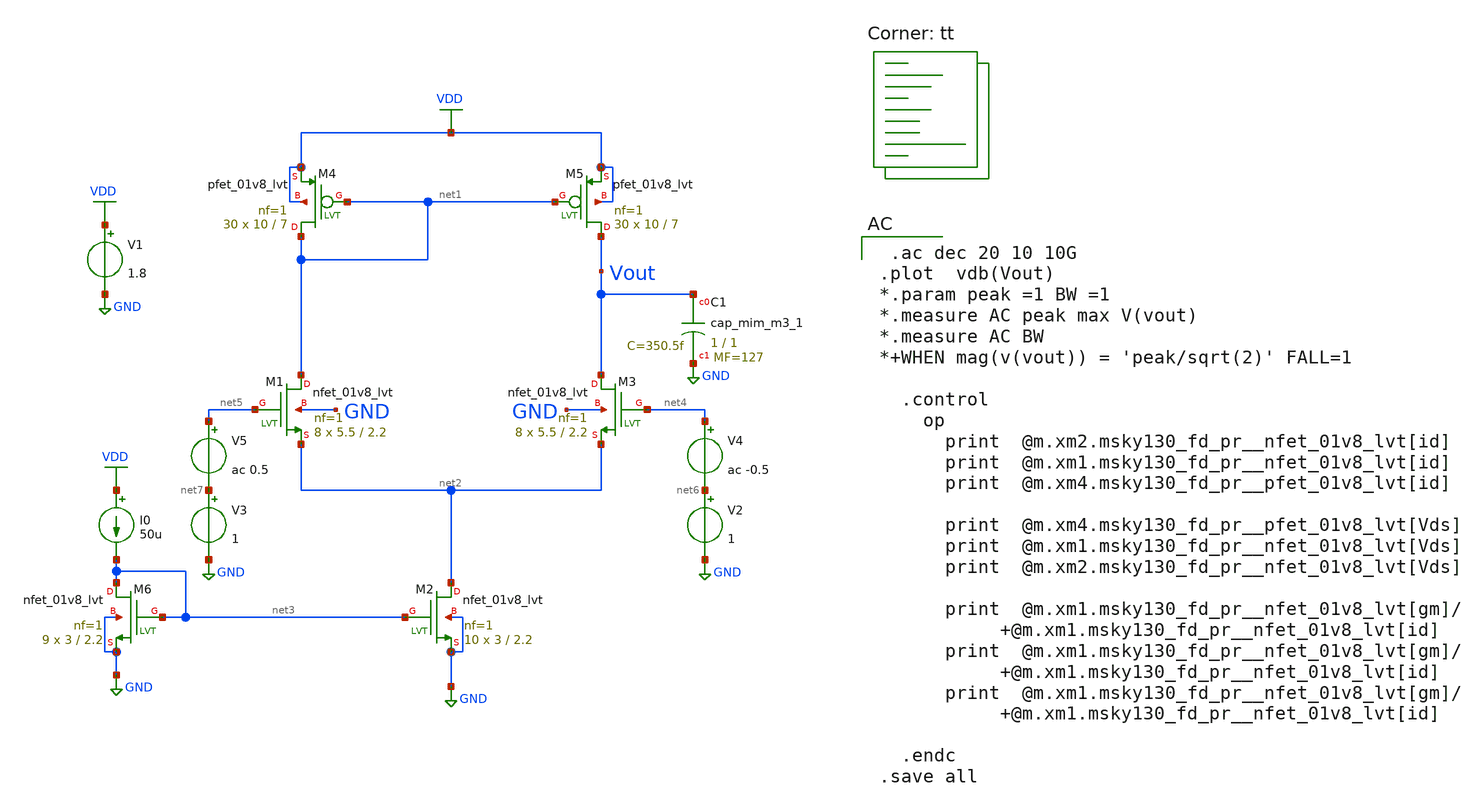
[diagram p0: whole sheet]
** sch_path: pll/lc_vco_lib_Hossam_Tarek/OTA/xschem/OTA.sch
**.subckt OTA
XM1 net1 net5 net2 GND sky130_fd_pr__nfet_01v8_lvt L=2.2 W=5.5 nf=1 ad='int((nf+1)/2) * W/nf * 0.29'
+ as='int((nf+2)/2) * W/nf * 0.29' pd='2*int((nf+1)/2) * (W/nf + 0.29)' ps='2*int((nf+2)/2) * (W/nf + 0.29)'
+ nrd='0.29 / W' nrs='0.29 / W' sa=0 sb=0 sd=0 mult=8 m=8
XM2 net2 net3 GND GND sky130_fd_pr__nfet_01v8_lvt L=2.2 W=3 nf=1 ad='int((nf+1)/2) * W/nf * 0.29' as='int((nf+2)/2) * W/nf * 0.29'
+ pd='2*int((nf+1)/2) * (W/nf + 0.29)' ps='2*int((nf+2)/2) * (W/nf + 0.29)' nrd='0.29 / W' nrs='0.29 / W'
+ sa=0 sb=0 sd=0 mult=10 m=10
XM3 Vout net4 net2 GND sky130_fd_pr__nfet_01v8_lvt L=2.2 W=5.5 nf=1 ad='int((nf+1)/2) * W/nf * 0.29'
+ as='int((nf+2)/2) * W/nf * 0.29' pd='2*int((nf+1)/2) * (W/nf + 0.29)' ps='2*int((nf+2)/2) * (W/nf + 0.29)'
+ nrd='0.29 / W' nrs='0.29 / W' sa=0 sb=0 sd=0 mult=8 m=8
XM4 net1 net1 VDD VDD sky130_fd_pr__pfet_01v8_lvt L=7 W=10 nf=1 ad='int((nf+1)/2) * W/nf * 0.29' as='int((nf+2)/2) * W/nf * 0.29'
+ pd='2*int((nf+1)/2) * (W/nf + 0.29)' ps='2*int((nf+2)/2) * (W/nf + 0.29)' nrd='0.29 / W' nrs='0.29 / W'
+ sa=0 sb=0 sd=0 mult=30 m=30
XM5 Vout net1 VDD VDD sky130_fd_pr__pfet_01v8_lvt L=7 W=10 nf=1 ad='int((nf+1)/2) * W/nf * 0.29' as='int((nf+2)/2) * W/nf * 0.29'
+ pd='2*int((nf+1)/2) * (W/nf + 0.29)' ps='2*int((nf+2)/2) * (W/nf + 0.29)' nrd='0.29 / W' nrs='0.29 / W'
+ sa=0 sb=0 sd=0 mult=30 m=30
V1 VDD GND 1.8
XM6 net3 net3 GND GND sky130_fd_pr__nfet_01v8_lvt L=2.2 W=3 nf=1 ad='int((nf+1)/2) * W/nf * 0.29' as='int((nf+2)/2) * W/nf * 0.29'
+ pd='2*int((nf+1)/2) * (W/nf + 0.29)' ps='2*int((nf+2)/2) * (W/nf + 0.29)' nrd='0.29 / W' nrs='0.29 / W'
+ sa=0 sb=0 sd=0 mult=9 m=9
I0 VDD net3 50u
V2 net6 GND 1
V4 net4 net6 ac -0.5
V3 net7 GND 1
V5 net5 net7 ac 0.5
XC1 Vout GND sky130_fd_pr__cap_mim_m3_1 W=1 L=1 MF=127 m=127
**** begin user architecture code
.lib $::SKYWATER_MODELS/sky130.lib.spice tt

 .ac dec 20 10 10G
.plot  vdb(Vout)
*.param peak =1 BW =1
*.measure AC peak max V(vout)
*.measure AC BW
*+WHEN mag(v(vout)) = 'peak/sqrt(2)' FALL=1

  .control
    op
      print  @m.xm2.msky130_fd_pr__nfet_01v8_lvt[id]
      print  @m.xm1.msky130_fd_pr__nfet_01v8_lvt[id]
      print  @m.xm4.msky130_fd_pr__pfet_01v8_lvt[id]

      print  @m.xm4.msky130_fd_pr__pfet_01v8_lvt[Vds]
      print  @m.xm1.msky130_fd_pr__nfet_01v8_lvt[Vds]
      print  @m.xm2.msky130_fd_pr__nfet_01v8_lvt[Vds]

      print  @m.xm1.msky130_fd_pr__nfet_01v8_lvt[gm]/
           +@m.xm1.msky130_fd_pr__nfet_01v8_lvt[id]
      print  @m.xm1.msky130_fd_pr__nfet_01v8_lvt[gm]/
           +@m.xm1.msky130_fd_pr__nfet_01v8_lvt[id]
      print  @m.xm1.msky130_fd_pr__nfet_01v8_lvt[gm]/
           +@m.xm1.msky130_fd_pr__nfet_01v8_lvt[id]

  .endc
.save all

**** end user architecture code
**.ends
.GLOBAL GND
.GLOBAL VDD
.end
